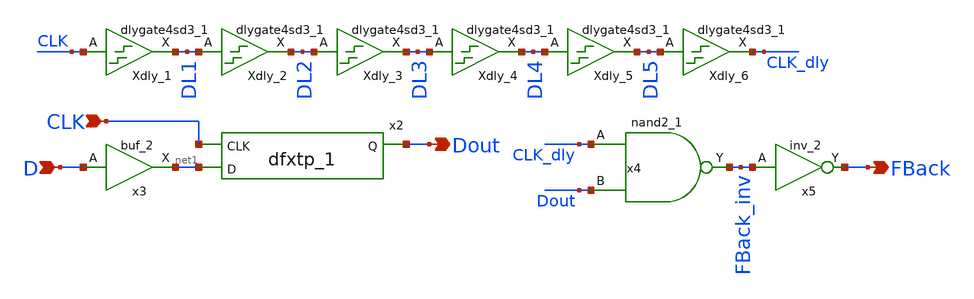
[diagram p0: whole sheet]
** sch_path: xschem/lib/DLib_Quantizer.sch
**.subckt DLib_Quantizer CLK D Dout FBack
*.ipin CLK
*.ipin D
*.opin Dout
*.opin FBack
Xdly_1 CLK VGND VNB VPB VPWR DL1 sky130_fd_sc_hd__dlygate4sd3_1
x2 CLK net1 VGND VNB VPB VPWR Dout sky130_fd_sc_hd__dfxtp_1
x3 D VGND VNB VPB VPWR net1 sky130_fd_sc_hd__buf_2
x4 CLK_dly Dout VGND VNB VPB VPWR FBack_inv sky130_fd_sc_hd__nand2_1
x5 FBack_inv VGND VNB VPB VPWR FBack sky130_fd_sc_hd__inv_2
Xdly_2 DL1 VGND VNB VPB VPWR DL2 sky130_fd_sc_hd__dlygate4sd3_1
Xdly_3 DL2 VGND VNB VPB VPWR DL3 sky130_fd_sc_hd__dlygate4sd3_1
Xdly_4 DL3 VGND VNB VPB VPWR DL4 sky130_fd_sc_hd__dlygate4sd3_1
Xdly_5 DL4 VGND VNB VPB VPWR DL5 sky130_fd_sc_hd__dlygate4sd3_1
Xdly_6 DL5 VGND VNB VPB VPWR CLK_dly sky130_fd_sc_hd__dlygate4sd3_1
**.ends
.end
